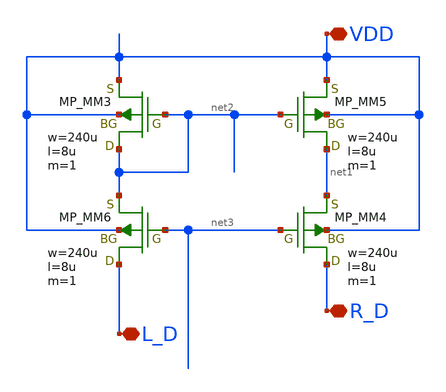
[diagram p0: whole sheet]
** sch_path: member_project/AM_Radio/noritsuna/xschem/CM_PMOS_base.sch
**.subckt CM_PMOS_base VDD L_D R_D
*.iopin VDD
*.iopin L_D
*.iopin R_D
MM3 net2 net2 VDD VDD PMOS w=240u l=8u as=0 ad=0 ps=0 pd=0 nrd=0 nrs=0 m=1
MM4 R_D net3 net1 VDD PMOS w=240u l=8u as=0 ad=0 ps=0 pd=0 nrd=0 nrs=0 m=1
MM5 net1 net2 VDD VDD PMOS w=240u l=8u as=0 ad=0 ps=0 pd=0 nrd=0 nrs=0 m=1
MM6 L_D net3 net2 VDD PMOS w=240u l=8u as=0 ad=0 ps=0 pd=0 nrd=0 nrs=0 m=1
**.ends
.end
